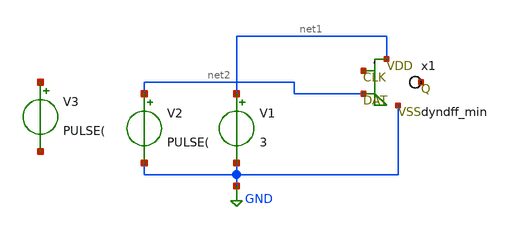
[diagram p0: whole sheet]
** sch_path: xschem/untitled.sch
**.subckt untitled
x1 net3 net2 net1 GND net4 dyndff_min
V1 net1 GND 3
V2 net2 GND PULSE(
V3 net5 net6 PULSE(
**.ends

* expanding   symbol:  dyndff_min.sym # of pins=5
** sym_path: xschem/dyndff_min.sym
** sch_path: xschem/dyndff_min.sch
.subckt dyndff_min CLK DAT VDD VSS Q
*.iopin DAT
*.iopin CLK
*.iopin Q
*.iopin VDD
*.iopin VSS
M1 net2 net1 VDD VDD pch w=30.0U l=10.0U as=0 ps=0 ad=0 pd=0 m=1
M2 net3 net5 VDD VDD pch w=30.0U l=10.0U as=0 ps=0 ad=0 pd=0 m=1
M3 net2 net1 VSS VSS nch w=10.0U l=10.0U as=0 ps=0 ad=0 pd=0 m=1
M4 net8 net1 net4 VSS nch w=10.0U l=10.0U as=0 ps=0 ad=0 pd=0 m=1
M5 net8 net2 net3 VDD pch w=30.0U l=10.0U as=0 ps=0 ad=0 pd=0 m=1
M6 net4 net5 VSS VSS nch w=10.0U l=10.0U as=0 ps=0 ad=0 pd=0 m=1
M7 net6 net8 VDD VDD pch w=30.0U l=10.0U as=0 ps=0 ad=0 pd=0 m=1
M8 int2 net1 net6 VDD pch w=30.0U l=10.0U as=0 ps=0 ad=0 pd=0 m=1
M9 int2 net2 net7 VSS nch w=10.0U l=10.0U as=0 ps=0 ad=0 pd=0 m=1
M10 net7 net8 VSS VSS nch w=10.0U l=10.0U as=0 ps=0 ad=0 pd=0 m=1
M11 Q int2 VDD VDD pch w=30.0U l=10.0U as=0 ps=0 ad=0 pd=0 m=1
M12 Q int2 VSS VSS nch w=10.0U l=10.0U as=0 ps=0 ad=0 pd=0 m=1
M13 net5 DAT VDD VDD pch w=30.0U l=10.0U as=0 ps=0 ad=0 pd=0 m=1
M14 net5 DAT VSS VSS nch w=10.0U l=10.0U as=0 ps=0 ad=0 pd=0 m=1
M15 net1 CLK VDD VDD pch w=30.0U l=10.0U as=0 ps=0 ad=0 pd=0 m=1
M16 net1 CLK VSS VSS nch w=10.0U l=10.0U as=0 ps=0 ad=0 pd=0 m=1
.ends

.GLOBAL GND
.end
